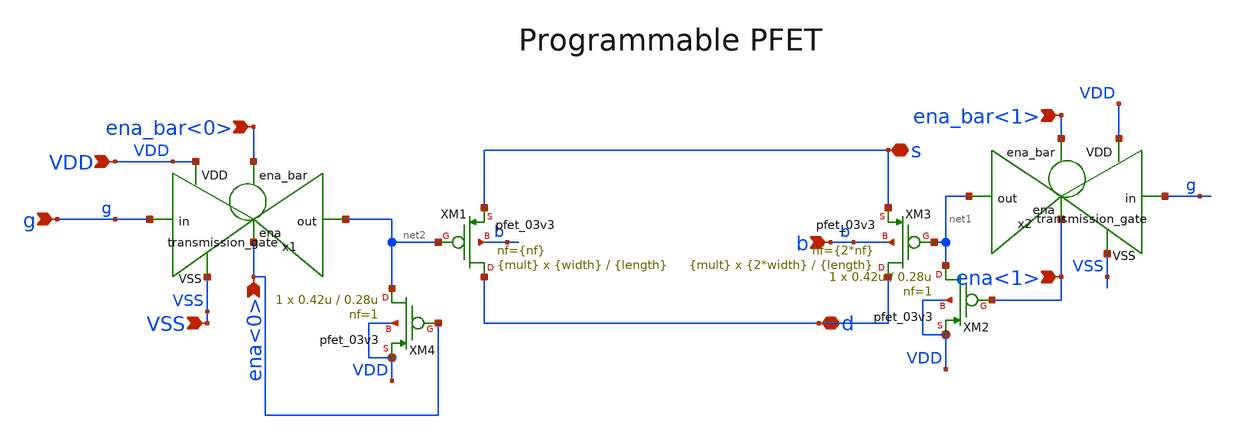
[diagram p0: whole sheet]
** sch_path: designs/libs/core_digital/schem/programmable_pfet.sch
**.subckt programmable_pfet VSS VDD g ena_bar<1> ena_bar<0> ena<0> s d b ena<1>
*.ipin VSS
*.ipin VDD
*.ipin g
*.ipin ena_bar<1>
*.ipin ena_bar<0>
*.ipin ena<0>
*.iopin s
*.iopin d
*.ipin b
*.ipin ena<1>
XM1 d net2 s b pfet_03v3 L={length} W={width} nf={nf} ad='int((nf+1)/2) * W/nf * 0.18u' as='int((nf+2)/2) * W/nf * 0.18u'
+ pd='2*int((nf+1)/2) * (W/nf + 0.18u)' ps='2*int((nf+2)/2) * (W/nf + 0.18u)' nrd='0.18u / W' nrs='0.18u / W'
+ sa=0 sb=0 sd=0 m={mult}
XM3 d net1 s b pfet_03v3 L={length} W={2*width} nf={2*nf} ad='int((nf+1)/2) * W/nf * 0.18u' as='int((nf+2)/2) * W/nf * 0.18u'
+ pd='2*int((nf+1)/2) * (W/nf + 0.18u)' ps='2*int((nf+2)/2) * (W/nf + 0.18u)' nrd='0.18u / W' nrs='0.18u / W'
+ sa=0 sb=0 sd=0 m={mult}
XM2 net1 ena<1> VDD VDD pfet_03v3 L=0.28u W=0.42u nf=1 ad='int((nf+1)/2) * W/nf * 0.18u' as='int((nf+2)/2) * W/nf * 0.18u'
+ pd='2*int((nf+1)/2) * (W/nf + 0.18u)' ps='2*int((nf+2)/2) * (W/nf + 0.18u)' nrd='0.18u / W' nrs='0.18u / W'
+ sa=0 sb=0 sd=0 m=1
XM4 net2 ena<0> VDD VDD pfet_03v3 L=0.28u W=0.42u nf=1 ad='int((nf+1)/2) * W/nf * 0.18u' as='int((nf+2)/2) * W/nf * 0.18u'
+ pd='2*int((nf+1)/2) * (W/nf + 0.18u)' ps='2*int((nf+2)/2) * (W/nf + 0.18u)' nrd='0.18u / W' nrs='0.18u / W'
+ sa=0 sb=0 sd=0 m=1
x1 ena_bar<0> VDD net2 g VSS ena<0> transmission_gate
x2 ena_bar<1> VDD net1 g VSS ena<1> transmission_gate
**.ends

* expanding   symbol:  libs/core_digital/schem/transmission_gate.sym # of pins=6
** sym_path: designs/libs/core_digital/schem/transmission_gate.sym
** sch_path: designs/libs/core_digital/schem/transmission_gate.sch
.subckt transmission_gate ena_bar VDD out in VSS ena
*.ipin in
*.ipin ena_bar
*.ipin ena
*.ipin VSS
*.ipin VDD
*.opin out
XM1 in ena_bar out VDD pfet_03v3 L=0.28u W=0.22u nf=1 ad='int((nf+1)/2) * W/nf * 0.18u' as='int((nf+2)/2) * W/nf * 0.18u'
+ pd='2*int((nf+1)/2) * (W/nf + 0.18u)' ps='2*int((nf+2)/2) * (W/nf + 0.18u)' nrd='0.18u / W' nrs='0.18u / W'
+ sa=0 sb=0 sd=0 m=1
XM2 in ena out VSS nfet_03v3 L=0.28u W=0.22u nf=1 ad='int((nf+1)/2) * W/nf * 0.18u' as='int((nf+2)/2) * W/nf * 0.18u'
+ pd='2*int((nf+1)/2) * (W/nf + 0.18u)' ps='2*int((nf+2)/2) * (W/nf + 0.18u)' nrd='0.18u / W' nrs='0.18u / W'
+ sa=0 sb=0 sd=0 m=1
.ends

.end
